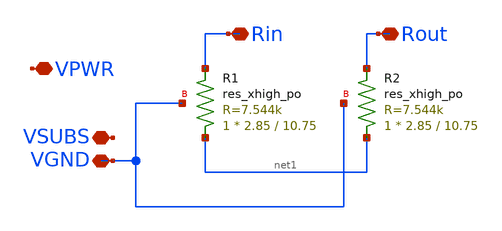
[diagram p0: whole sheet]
** sch_path: xschem/multiple_bgr/sky130_asc_res_xhigh_po_2p85_2.sch
**.subckt sky130_asc_res_xhigh_po_2p85_2 Rin Rout VPWR VSUBS VGND
*.iopin Rin
*.iopin Rout
*.iopin VPWR
*.iopin VSUBS
*.iopin VGND
XR1 net1 Rin VGND sky130_fd_pr__res_xhigh_po W=2.85 L=10.75 mult=1 m=1
XR2 net1 Rout VGND sky130_fd_pr__res_xhigh_po W=2.85 L=10.75 mult=1 m=1
**.ends
.end
